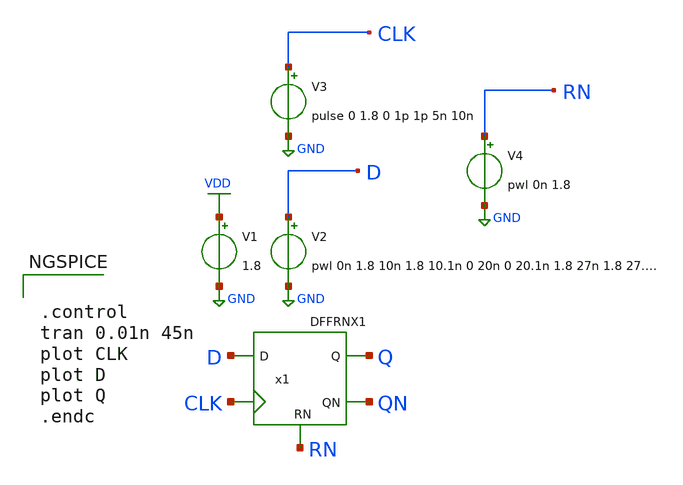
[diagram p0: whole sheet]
** sch_path: lib/xschem/test_DFFRNX1.sch
**.subckt test_DFFRNX1
V2 D GND pwl 0n 1.8 10n 1.8 10.1n 0 20n 0 20.1n 1.8 27n 1.8 27.1n 0 34n 0 34.1n 1.8
V1 VDD GND 1.8
V3 CLK GND pulse 0 1.8 0 1p 1p 5n 10n
V4 RN GND pwl 0n 1.8
x1 Q QN D CLK RN VDD GND DFFRNX1
**** begin user architecture code

.lib $::SKYWATER_MODELS/sky130.lib.spice tt


**** end user architecture code
**.ends

* expanding   symbol:  DFFRNX1.sym # of pins=5
** sym_path: DFFRNX1.sym
** sch_path: DFFRNX1.sch
.subckt DFFRNX1 Q QN D CLK RN VDD VSS
*.ipin D
*.opin QN
*.ipin RN
*.ipin CLK
*.opin Q
x2 net4 net1 RN D VDD VSS NAND3X1
x1 net1 net3 CLK net4 VDD VSS NAND3X1
x3 net2 net4 net3 VDD VSS NAND2X1
x4 net3 net2 CLK RN VDD VSS NAND3X1
x5 QN net1 RN Q VDD VSS NAND3X1
x6 Q QN net3 VDD VSS NAND2X1
.ends


* expanding   symbol:  NAND3X1.sym # of pins=4
** sym_path: lib/xschem/NAND3X1.sym
** sch_path: lib/xschem/NAND3X1.sch
.subckt NAND3X1 Y A B C VDD VSS
*.ipin A
*.opin Y
*.ipin B
*.ipin C
XM1 net2 C VSS VSS sky130_fd_pr__nfet_01v8 L=0.15 W=3 nf=1 ad='int((nf+1)/2) * W/nf * 0.29' as='int((nf+2)/2) * W/nf * 0.29'
+ pd='2*int((nf+1)/2) * (W/nf + 0.29)' ps='2*int((nf+2)/2) * (W/nf + 0.29)' nrd='0.29 / W' nrs='0.29 / W'
+ sa=0 sb=0 sd=0 mult=1 m=1
XM2 Y A VDD VDD sky130_fd_pr__pfet_01v8 L=0.15 W=2 nf=1 ad='int((nf+1)/2) * W/nf * 0.29' as='int((nf+2)/2) * W/nf * 0.29'
+ pd='2*int((nf+1)/2) * (W/nf + 0.29)' ps='2*int((nf+2)/2) * (W/nf + 0.29)' nrd='0.29 / W' nrs='0.29 / W'
+ sa=0 sb=0 sd=0 mult=1 m=1
XM3 net1 B net2 VSS sky130_fd_pr__nfet_01v8 L=0.15 W=3 nf=1 ad='int((nf+1)/2) * W/nf * 0.29' as='int((nf+2)/2) * W/nf * 0.29'
+ pd='2*int((nf+1)/2) * (W/nf + 0.29)' ps='2*int((nf+2)/2) * (W/nf + 0.29)' nrd='0.29 / W' nrs='0.29 / W'
+ sa=0 sb=0 sd=0 mult=1 m=1
XM4 Y A net1 VSS sky130_fd_pr__nfet_01v8 L=0.15 W=3 nf=1 ad='int((nf+1)/2) * W/nf * 0.29' as='int((nf+2)/2) * W/nf * 0.29'
+ pd='2*int((nf+1)/2) * (W/nf + 0.29)' ps='2*int((nf+2)/2) * (W/nf + 0.29)' nrd='0.29 / W' nrs='0.29 / W'
+ sa=0 sb=0 sd=0 mult=1 m=1
XM5 Y A VDD VDD sky130_fd_pr__pfet_01v8 L=0.15 W=2 nf=1 ad='int((nf+1)/2) * W/nf * 0.29' as='int((nf+2)/2) * W/nf * 0.29'
+ pd='2*int((nf+1)/2) * (W/nf + 0.29)' ps='2*int((nf+2)/2) * (W/nf + 0.29)' nrd='0.29 / W' nrs='0.29 / W'
+ sa=0 sb=0 sd=0 mult=1 m=1
XM6 Y B VDD VDD sky130_fd_pr__pfet_01v8 L=0.15 W=2 nf=1 ad='int((nf+1)/2) * W/nf * 0.29' as='int((nf+2)/2) * W/nf * 0.29'
+ pd='2*int((nf+1)/2) * (W/nf + 0.29)' ps='2*int((nf+2)/2) * (W/nf + 0.29)' nrd='0.29 / W' nrs='0.29 / W'
+ sa=0 sb=0 sd=0 mult=1 m=1
XM7 Y B VDD VDD sky130_fd_pr__pfet_01v8 L=0.15 W=2 nf=1 ad='int((nf+1)/2) * W/nf * 0.29' as='int((nf+2)/2) * W/nf * 0.29'
+ pd='2*int((nf+1)/2) * (W/nf + 0.29)' ps='2*int((nf+2)/2) * (W/nf + 0.29)' nrd='0.29 / W' nrs='0.29 / W'
+ sa=0 sb=0 sd=0 mult=1 m=1
XM8 Y C VDD VDD sky130_fd_pr__pfet_01v8 L=0.15 W=2 nf=1 ad='int((nf+1)/2) * W/nf * 0.29' as='int((nf+2)/2) * W/nf * 0.29'
+ pd='2*int((nf+1)/2) * (W/nf + 0.29)' ps='2*int((nf+2)/2) * (W/nf + 0.29)' nrd='0.29 / W' nrs='0.29 / W'
+ sa=0 sb=0 sd=0 mult=1 m=1
XM9 Y C VDD VDD sky130_fd_pr__pfet_01v8 L=0.15 W=2 nf=1 ad='int((nf+1)/2) * W/nf * 0.29' as='int((nf+2)/2) * W/nf * 0.29'
+ pd='2*int((nf+1)/2) * (W/nf + 0.29)' ps='2*int((nf+2)/2) * (W/nf + 0.29)' nrd='0.29 / W' nrs='0.29 / W'
+ sa=0 sb=0 sd=0 mult=1 m=1
.ends


* expanding   symbol:  NAND2X1.sym # of pins=3
** sym_path: lib/xschem/NAND2X1.sym
** sch_path: lib/xschem/NAND2X1.sch
.subckt NAND2X1 Y A B VDD VSS
*.ipin A
*.opin Y
*.ipin B
XM1 Y A VDD VDD sky130_fd_pr__pfet_01v8 L=0.15 W=2 nf=1 ad='int((nf+1)/2) * W/nf * 0.29' as='int((nf+2)/2) * W/nf * 0.29'
+ pd='2*int((nf+1)/2) * (W/nf + 0.29)' ps='2*int((nf+2)/2) * (W/nf + 0.29)' nrd='0.29 / W' nrs='0.29 / W'
+ sa=0 sb=0 sd=0 mult=1 m=1
XM5 Y A net1 VSS sky130_fd_pr__nfet_01v8 L=0.15 W=3 nf=1 ad='int((nf+1)/2) * W/nf * 0.29' as='int((nf+2)/2) * W/nf * 0.29'
+ pd='2*int((nf+1)/2) * (W/nf + 0.29)' ps='2*int((nf+2)/2) * (W/nf + 0.29)' nrd='0.29 / W' nrs='0.29 / W'
+ sa=0 sb=0 sd=0 mult=1 m=1
XM2 Y A VDD VDD sky130_fd_pr__pfet_01v8 L=0.15 W=2 nf=1 ad='int((nf+1)/2) * W/nf * 0.29' as='int((nf+2)/2) * W/nf * 0.29'
+ pd='2*int((nf+1)/2) * (W/nf + 0.29)' ps='2*int((nf+2)/2) * (W/nf + 0.29)' nrd='0.29 / W' nrs='0.29 / W'
+ sa=0 sb=0 sd=0 mult=1 m=1
XM3 Y B VDD VDD sky130_fd_pr__pfet_01v8 L=0.15 W=2 nf=1 ad='int((nf+1)/2) * W/nf * 0.29' as='int((nf+2)/2) * W/nf * 0.29'
+ pd='2*int((nf+1)/2) * (W/nf + 0.29)' ps='2*int((nf+2)/2) * (W/nf + 0.29)' nrd='0.29 / W' nrs='0.29 / W'
+ sa=0 sb=0 sd=0 mult=1 m=1
XM4 Y B VDD VDD sky130_fd_pr__pfet_01v8 L=0.15 W=2 nf=1 ad='int((nf+1)/2) * W/nf * 0.29' as='int((nf+2)/2) * W/nf * 0.29'
+ pd='2*int((nf+1)/2) * (W/nf + 0.29)' ps='2*int((nf+2)/2) * (W/nf + 0.29)' nrd='0.29 / W' nrs='0.29 / W'
+ sa=0 sb=0 sd=0 mult=1 m=1
XM6 net1 B VSS VSS sky130_fd_pr__nfet_01v8 L=0.15 W=3 nf=1 ad='int((nf+1)/2) * W/nf * 0.29' as='int((nf+2)/2) * W/nf * 0.29'
+ pd='2*int((nf+1)/2) * (W/nf + 0.29)' ps='2*int((nf+2)/2) * (W/nf + 0.29)' nrd='0.29 / W' nrs='0.29 / W'
+ sa=0 sb=0 sd=0 mult=1 m=1
.ends

.GLOBAL VDD
.GLOBAL GND
**** begin user architecture code


.control
tran 0.01n 45n
plot CLK
plot D
plot Q
.endc


**** end user architecture code
.end
